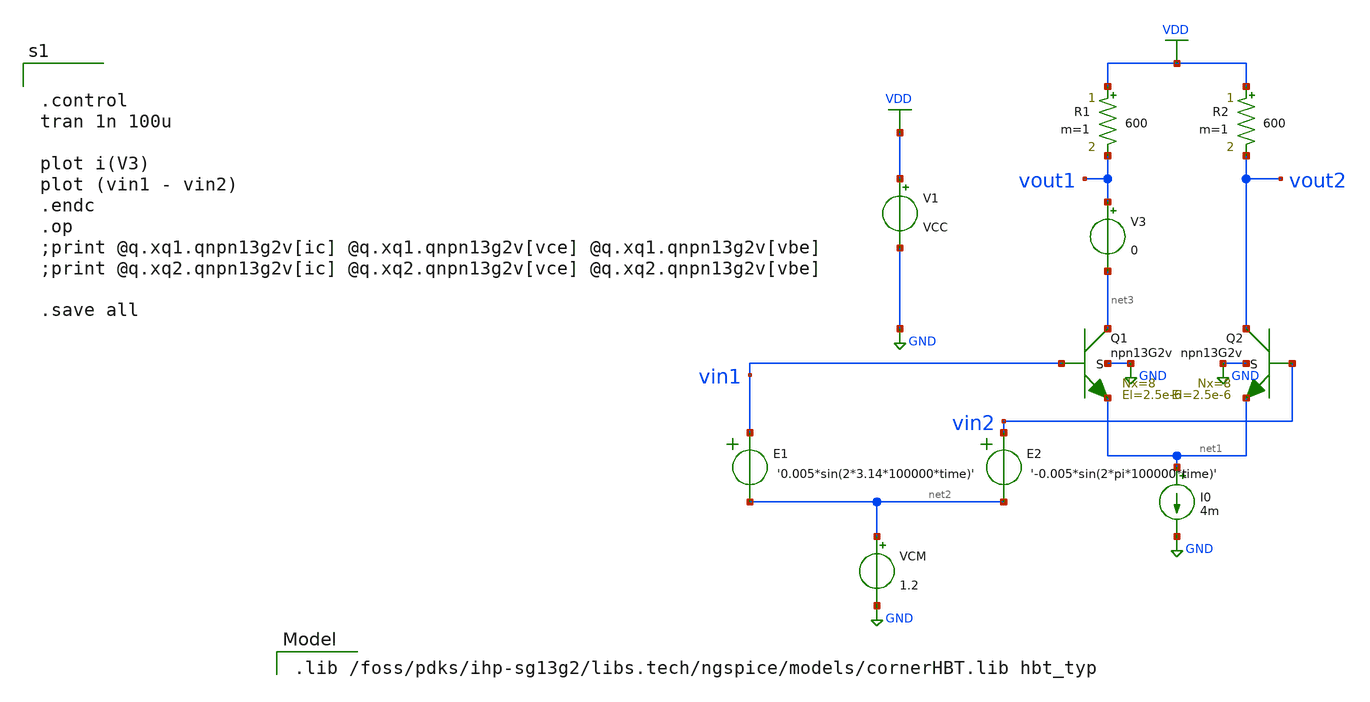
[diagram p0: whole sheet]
** sch_path: sim_backup/simulations/LNA_new.sch
**.subckt LNA_new
V1 VDD GND VCC
XQ1 net3 vin1 net1 GND npn13G2v Nx=8 El=2.5e-6 mm_ok=1
XQ2 vout2 vin2 net1 GND npn13G2v Nx=8 El=2.5e-6 mm_ok=1
I0 net1 GND 4m
R1 VDD vout1 600 m=1
R2 VDD vout2 600 m=1
VCM net2 GND 1.2
E1 vin1 net2 VOL=' '0.005*sin(2*3.14*100000*time)' '
E2 vin2 net2 VOL=' '-0.005*sin(2*pi*100000*time)' '
V3 vout1 net3 0
**** begin user architecture code


.control
tran 1n 100u

plot i(V3)
plot (vin1 - vin2)
.endc
.op
;print @q.xq1.qnpn13g2v[ic] @q.xq1.qnpn13g2v[vce] @q.xq1.qnpn13g2v[vbe]
;print @q.xq2.qnpn13g2v[ic] @q.xq2.qnpn13g2v[vce] @q.xq2.qnpn13g2v[vbe]

.save all



.lib /foss/pdks/ihp-sg13g2/libs.tech/ngspice/models/cornerHBT.lib hbt_typ

**** end user architecture code
**.ends
.GLOBAL VDD
.GLOBAL GND
.end
